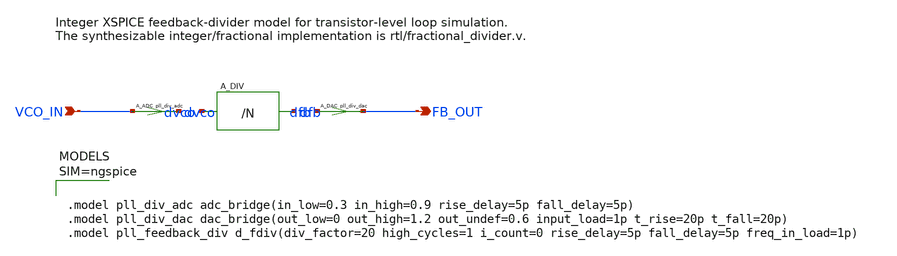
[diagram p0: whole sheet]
** sch_path: schematic/xschem/pll/feedback_divider.sch
**.subckt feedback_divider VCO_IN FB_OUT
*.ipin VCO_IN
*.opin FB_OUT
A_ADC [ VCO_IN ] [ dvco ] pll_div_adc
A_DIV dvco dfb pll_feedback_div
A_DAC [ dfb ] [ FB_OUT ] pll_div_dac
**** begin user architecture code



.model pll_div_adc adc_bridge(in_low=0.3 in_high=0.9 rise_delay=5p fall_delay=5p)
.model pll_div_dac dac_bridge(out_low=0 out_high=1.2 out_undef=0.6 input_load=1p t_rise=20p
+ t_fall=20p)
.model pll_feedback_div d_fdiv(div_factor=20 high_cycles=1 i_count=0 rise_delay=5p fall_delay=5p
+ freq_in_load=1p)



**** end user architecture code
**.ends
.end
